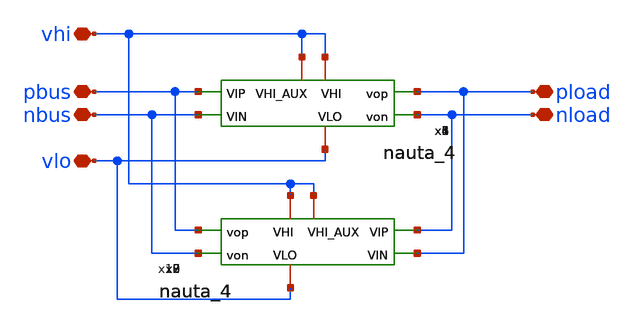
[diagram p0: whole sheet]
** sch_path: xschem/gyrator.sch
**.subckt gyrator nbus pbus vhi vlo pload nload
*.iopin nbus
*.iopin pbus
*.iopin vhi
*.iopin vlo
*.iopin pload
*.iopin nload
x1 vhi vhi pbus pload nbus nload vlo nauta_4
x2 vhi vhi nload pbus pload nbus vlo nauta_4
x3 vhi vhi pbus pload nbus nload vlo nauta_4
x4 vhi vhi pbus pload nbus nload vlo nauta_4
x5 vhi vhi pbus pload nbus nload vlo nauta_4
x6 vhi vhi pbus pload nbus nload vlo nauta_4
x7 vhi vhi nload pbus pload nbus vlo nauta_4
x8 vhi vhi nload pbus pload nbus vlo nauta_4
x9 vhi vhi nload pbus pload nbus vlo nauta_4
x10 vhi vhi nload pbus pload nbus vlo nauta_4
**.ends

* expanding   symbol:  nauta_4.sym # of pins=7
** sym_path: xschem/nauta_4.sym
** sch_path: xschem/nauta_4.sch
.subckt nauta_4 VHI_AUX VHI VIP vop VIN von VLO
*.ipin VIP
*.ipin VIN
*.opin vop
*.opin von
*.iopin VHI
*.iopin VHI_AUX
*.iopin VLO
**** begin user architecture code

.subckt NAUTA VOP VON VIP VIN VHI VHI_AUX VLO

XA0N VON VIP VLO VLO nmos_6p0 w=0.82u l=0.6u
XA0P VON VIP VHI VHI pmos_6p0 w=1.22u l=0.5u
XA1N VON VIP VLO VLO nmos_6p0 w=0.82u l=0.6u
XA1P VON VIP VHI VHI pmos_6p0 w=1.22u l=0.5u

XB0N VOP VIN VLO VLO nmos_6p0 w=0.82u l=0.6u
XB0P VOP VIN VHI VHI pmos_6p0 w=1.22u l=0.5u
XB1N VOP VIN VLO VLO nmos_6p0 w=0.82u l=0.6u
XB1P VOP VIN VHI VHI pmos_6p0 w=1.22u l=0.5u

XC0N VOP VON VLO VLO nmos_6p0 w=0.82u l=0.6u
XC0P VOP VON VHI VHI pmos_6p0 w=1.22u l=0.5u

XD0N VON VOP VLO VLO nmos_6p0 w=0.82u l=0.6u
XD0P VON VOP VHI VHI pmos_6p0 w=1.22u l=0.5u

XC1N VOP VOP VLO VLO nmos_6p0 w=0.82u l=0.6u
XC1P VOP VOP VHI_AUX VHI_AUX pmos_6p0 w=1.22u l=0.5u

XD1N VON VON VLO VLO nmos_6p0 w=0.82u l=0.6u
XD1P VON VON VHI_AUX VHI_AUX pmos_6p0 w=1.22u l=0.5u

.ends

XDUT VOP VON VIP VIN VHI VHI_AUX VLO NAUTA


**** end user architecture code
.ends

.end
